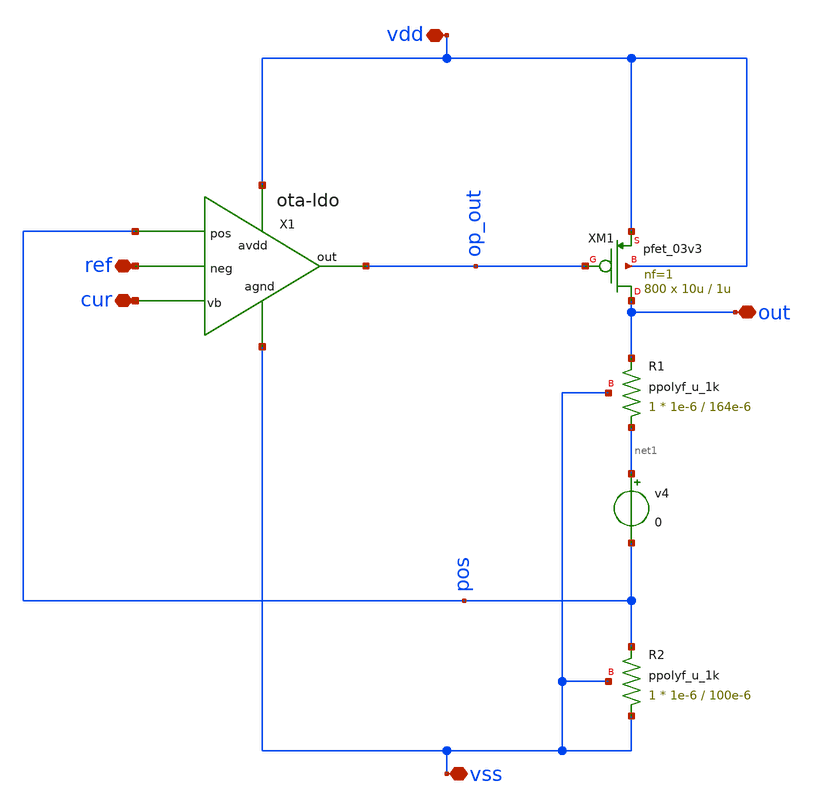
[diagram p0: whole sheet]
** sch_path: LDO/xschem/ldo/symbol/ldo.sch

.include $env(PDK_ROOT)/$env(PDK)/libs.tech/ngspice/design.ngspice
.lib $env(PDK_ROOT)/$env(PDK)/libs.tech/ngspice/sm141064.ngspice typical
.lib $env(PDK_ROOT)/$env(PDK)/libs.tech/ngspice/sm141064.ngspice mimcap_statistical
.lib $env(PDK_ROOT)/$env(PDK)/libs.tech/ngspice/sm141064.ngspice cap_mim
.lib $env(PDK_ROOT)/$env(PDK)/libs.tech/ngspice/sm141064.ngspice res_typical

**.subckt ldo ref out cur vss vdd
*.iopin ref
*.iopin out
*.iopin cur
*.iopin vss
*.iopin vdd
X1 vdd op_out ref pos cur vss ota-ldo
XM1 out op_out vdd vdd pfet_03v3 L=1u W=10u nf=1 ad='int((nf+1)/2) * W/nf * 0.18u' as='int((nf+2)/2) * W/nf * 0.18u'
+ pd='2*int((nf+1)/2) * (W/nf + 0.18u)' ps='2*int((nf+2)/2) * (W/nf + 0.18u)' nrd='0.18u / W' nrs='0.18u / W'
+ sa=0 sb=0 sd=0 m=800
XR1 net1 out vss ppolyf_u_1k r_width=1e-6 r_length=164e-6 m=1
XR2 vss pos vss ppolyf_u_1k r_width=1e-6 r_length=100e-6 m=1
v4 net1 pos 0
**.ends

* expanding   symbol:  symbol/ota-ldo.sym # of pins=6
** sym_path: LDO/xschem/ota-ldo/ota-ldo.sym
** sch_path: LDO/xschem/ota-ldo/ota-ldo.sch
.subckt ota-ldo avdd out neg pos vb agnd
*.iopin vb
*.iopin avdd
*.iopin agnd
*.ipin neg
*.ipin pos
*.opin out
XC2 net2 out cap_mim_1f5fF c_width=50e-6 c_length=20e-6 m=1
XM1 net1 neg net3 agnd nfet_03v3 L=0.3u W=10u nf=1 ad='int((nf+1)/2) * W/nf * 0.18u' as='int((nf+2)/2) * W/nf * 0.18u'
+ pd='2*int((nf+1)/2) * (W/nf + 0.18u)' ps='2*int((nf+2)/2) * (W/nf + 0.18u)' nrd='0.18u / W' nrs='0.18u / W'
+ sa=0 sb=0 sd=0 m=1
XM3 net1 net1 avdd avdd pfet_03v3 L=0.8u W=9u nf=1 ad='int((nf+1)/2) * W/nf * 0.18u' as='int((nf+2)/2) * W/nf * 0.18u'
+ pd='2*int((nf+1)/2) * (W/nf + 0.18u)' ps='2*int((nf+2)/2) * (W/nf + 0.18u)' nrd='0.18u / W' nrs='0.18u / W'
+ sa=0 sb=0 sd=0 m=1
XM2 net2 pos net3 agnd nfet_03v3 L=0.3u W=10u nf=1 ad='int((nf+1)/2) * W/nf * 0.18u' as='int((nf+2)/2) * W/nf * 0.18u'
+ pd='2*int((nf+1)/2) * (W/nf + 0.18u)' ps='2*int((nf+2)/2) * (W/nf + 0.18u)' nrd='0.18u / W' nrs='0.18u / W'
+ sa=0 sb=0 sd=0 m=1
XM4 net2 net1 avdd avdd pfet_03v3 L=0.8u W=9u nf=1 ad='int((nf+1)/2) * W/nf * 0.18u' as='int((nf+2)/2) * W/nf * 0.18u'
+ pd='2*int((nf+1)/2) * (W/nf + 0.18u)' ps='2*int((nf+2)/2) * (W/nf + 0.18u)' nrd='0.18u / W' nrs='0.18u / W'
+ sa=0 sb=0 sd=0 m=1
XM7 net3 vb agnd agnd nfet_03v3 L=0.8u W=16u nf=1 ad='int((nf+1)/2) * W/nf * 0.18u' as='int((nf+2)/2) * W/nf * 0.18u'
+ pd='2*int((nf+1)/2) * (W/nf + 0.18u)' ps='2*int((nf+2)/2) * (W/nf + 0.18u)' nrd='0.18u / W' nrs='0.18u / W'
+ sa=0 sb=0 sd=0 m=1
XM8 vb vb agnd agnd nfet_03v3 L=0.8u W=1.66u nf=1 ad='int((nf+1)/2) * W/nf * 0.18u' as='int((nf+2)/2) * W/nf * 0.18u'
+ pd='2*int((nf+1)/2) * (W/nf + 0.18u)' ps='2*int((nf+2)/2) * (W/nf + 0.18u)' nrd='0.18u / W' nrs='0.18u / W'
+ sa=0 sb=0 sd=0 m=1
XM5 out net2 avdd avdd pfet_03v3 L=0.4u W=60u nf=1 ad='int((nf+1)/2) * W/nf * 0.18u' as='int((nf+2)/2) * W/nf * 0.18u'
+ pd='2*int((nf+1)/2) * (W/nf + 0.18u)' ps='2*int((nf+2)/2) * (W/nf + 0.18u)' nrd='0.18u / W' nrs='0.18u / W'
+ sa=0 sb=0 sd=0 m=1
XM6 out vb agnd agnd nfet_03v3 L=0.8u W=60u nf=1 ad='int((nf+1)/2) * W/nf * 0.18u' as='int((nf+2)/2) * W/nf * 0.18u'
+ pd='2*int((nf+1)/2) * (W/nf + 0.18u)' ps='2*int((nf+2)/2) * (W/nf + 0.18u)' nrd='0.18u / W' nrs='0.18u / W'
+ sa=0 sb=0 sd=0 m=1
.ends

.end
